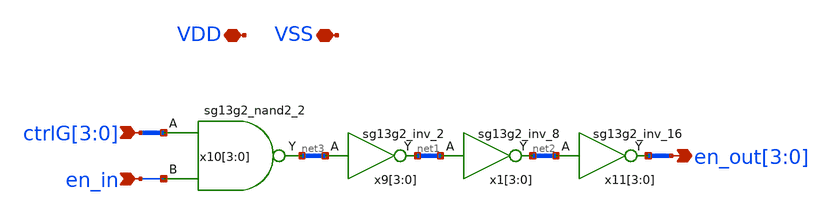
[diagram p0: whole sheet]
** sch_path: xschem/iruwbtx7_PA_decoder.sch
* IHP-GmbH/IHP-Open-PDK/ihp-sg13g2/libs.tech/xschem/sg13g2_stdcells/sg13g2_inv_16.sch:
* Copyright 2023 IHP PDK Authors
* Licensed under the Apache License, Version 2.0 (the "License");
**.subckt iruwbtx7_PA_decoder ctrlG[3],ctrlG[2],ctrlG[1],ctrlG[0] en_in
*+ en_out[3],en_out[2],en_out[1],en_out[0] VDD VSS
*.ipin ctrlG[3],ctrlG[2],ctrlG[1],ctrlG[0]
*.ipin en_in
*.opin en_out[3],en_out[2],en_out[1],en_out[0]
*.iopin VDD
*.iopin VSS
x10[3] net3[3] ctrlG[3] en_in VDD VSS sg13g2_nand2_2
x10[2] net3[2] ctrlG[2] en_in VDD VSS sg13g2_nand2_2
x10[1] net3[1] ctrlG[1] en_in VDD VSS sg13g2_nand2_2
x10[0] net3[0] ctrlG[0] en_in VDD VSS sg13g2_nand2_2
x9[3] net1[3] net3[3] VDD VSS sg13g2_inv_2
x9[2] net1[2] net3[2] VDD VSS sg13g2_inv_2
x9[1] net1[1] net3[1] VDD VSS sg13g2_inv_2
x9[0] net1[0] net3[0] VDD VSS sg13g2_inv_2
x1[3] net2[3] net1[3] VDD VSS sg13g2_inv_8
x1[2] net2[2] net1[2] VDD VSS sg13g2_inv_8
x1[1] net2[1] net1[1] VDD VSS sg13g2_inv_8
x1[0] net2[0] net1[0] VDD VSS sg13g2_inv_8
x11[3] en_out[3] net2[3] VDD VSS sg13g2_inv_16
x11[2] en_out[2] net2[2] VDD VSS sg13g2_inv_16
x11[1] en_out[1] net2[1] VDD VSS sg13g2_inv_16
x11[0] en_out[0] net2[0] VDD VSS sg13g2_inv_16
**.ends

* expanding   symbol:  sg13g2_nand2_2.sym # of pins=3
** sym_path: sg13g2_nand2_2.sym
** sch_path: sg13g2_nand2_2.sch
.subckt sg13g2_nand2_2 Y A B VDD VSS
*.iopin VDD
*.iopin VSS
*.opin Y
*.ipin B
*.ipin A
XM1 Y A net1 VSS sg13_lv_nmos w=1.44u l=130.00n ng=2 m=1 mm_ok=1
XM2 net1 B VSS VSS sg13_lv_nmos w=1.44u l=130.00n ng=2 m=1 mm_ok=1
XM3 Y A VDD VDD sg13_lv_pmos w=2.24u l=130.00n ng=2 m=1 mm_ok=1
XM4 Y B VDD VDD sg13_lv_pmos w=2.24u l=130.00n ng=2 m=1 mm_ok=1
.ends


* expanding   symbol:  sg13g2_inv_2.sym # of pins=2
** sym_path: sg13g2_inv_2.sym
** sch_path: sg13g2_inv_2.sch
.subckt sg13g2_inv_2 Y A VDD VSS
*.opin Y
*.ipin A
*.iopin VDD
*.iopin VSS
XM1 Y A VSS VSS sg13_lv_nmos w=1.48u l=130.00n ng=2 m=1 mm_ok=1
XM2 Y A VDD VDD sg13_lv_pmos w=2.24u l=130.00n ng=2 m=1 mm_ok=1
.ends


* expanding   symbol:  sg13g2_inv_8.sym # of pins=2
** sym_path: sg13g2_inv_8.sym
** sch_path: sg13g2_inv_8.sch
.subckt sg13g2_inv_8 Y A VDD VSS
*.opin Y
*.ipin A
*.iopin VDD
*.iopin VSS
XM1 Y A VSS VSS sg13_lv_nmos w=5.92u l=130.00n ng=8 m=1 mm_ok=1
XM2 Y A VDD VDD sg13_lv_pmos w=8.96u l=130.00n ng=8 m=1 mm_ok=1
.ends


* expanding   symbol:  sg13g2_inv_16.sym # of pins=2
** sym_path: sg13g2_inv_16.sym
** sch_path: sg13g2_inv_16.sch
.subckt sg13g2_inv_16 Y A VDD VSS
*.opin Y
*.iopin VSS
*.ipin A
*.iopin VDD
XM1 Y A VSS VSS sg13_lv_nmos w=11.84u l=130.00n ng=16 m=1 mm_ok=1
XM2 Y A VDD VDD sg13_lv_pmos w=17.92u l=130.00n ng=16 m=1 mm_ok=1
.ends

.end
